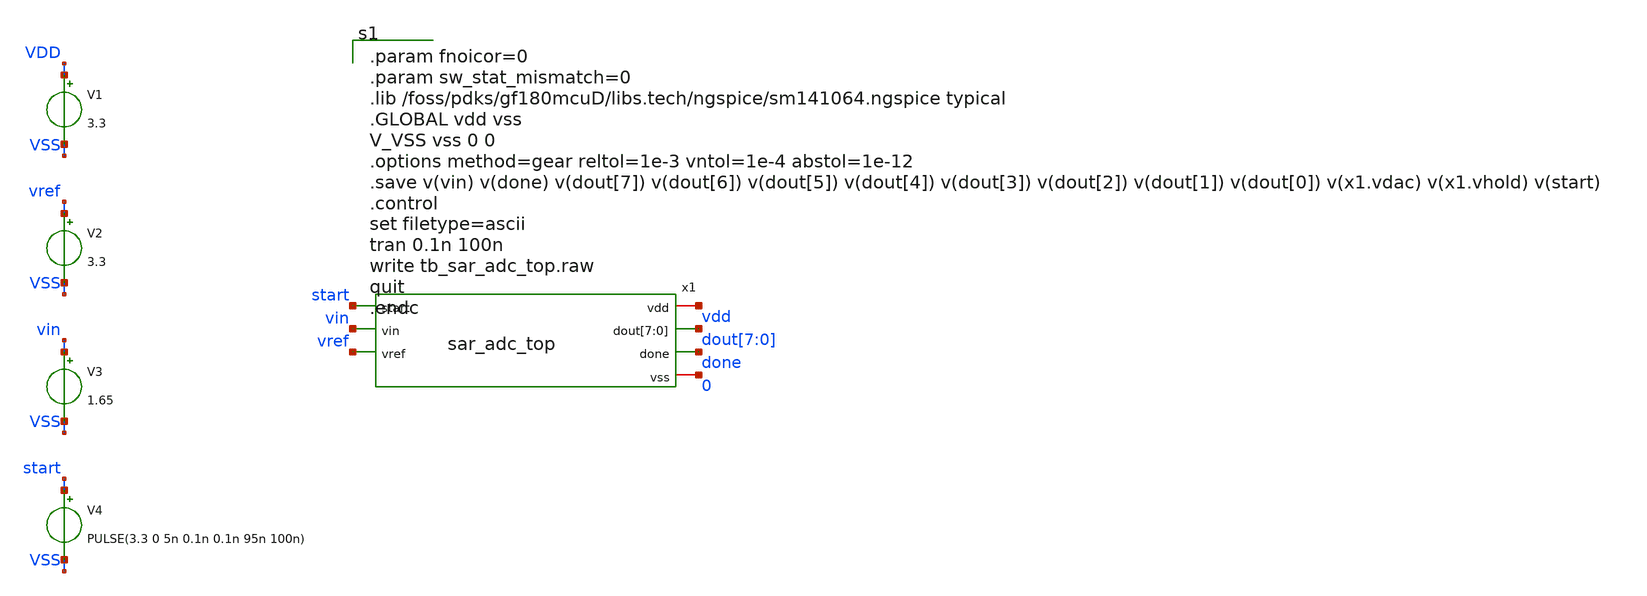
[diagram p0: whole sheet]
** sch_path: xschem/sar_adc/tb_sar_adc_top.sch
**.subckt tb_sar_adc_top
V1 VDD VSS 3.3
V2 vref VSS 3.3
V3 vin VSS 1.65
V4 start VSS PULSE(3.3 0 5n 0.1n 0.1n 95n 100n)
x1 vdd start vin dout[7] dout[6] dout[5] dout[4] dout[3] dout[2] dout[1] dout[0] done vref 0
+ sar_adc_top
**.ends
**** begin user architecture code

.param fnoicor=0
.param sw_stat_mismatch=0
.lib /foss/pdks/gf180mcuD/libs.tech/ngspice/sm141064.ngspice typical
.GLOBAL vdd vss
V_VSS vss 0 0
.options method=gear reltol=1e-3 vntol=1e-4 abstol=1e-12
.save v(vin) v(done) v(dout[7]) v(dout[6]) v(dout[5]) v(dout[4]) v(dout[3]) v(dout[2]) v(dout[1]) v(dout[0]) v(x1.vdac) v(x1.vhold) v(start)
.control
set filetype=ascii
tran 0.1n 100n
write tb_sar_adc_top.raw
quit
.endc

**** end user architecture code
.end
